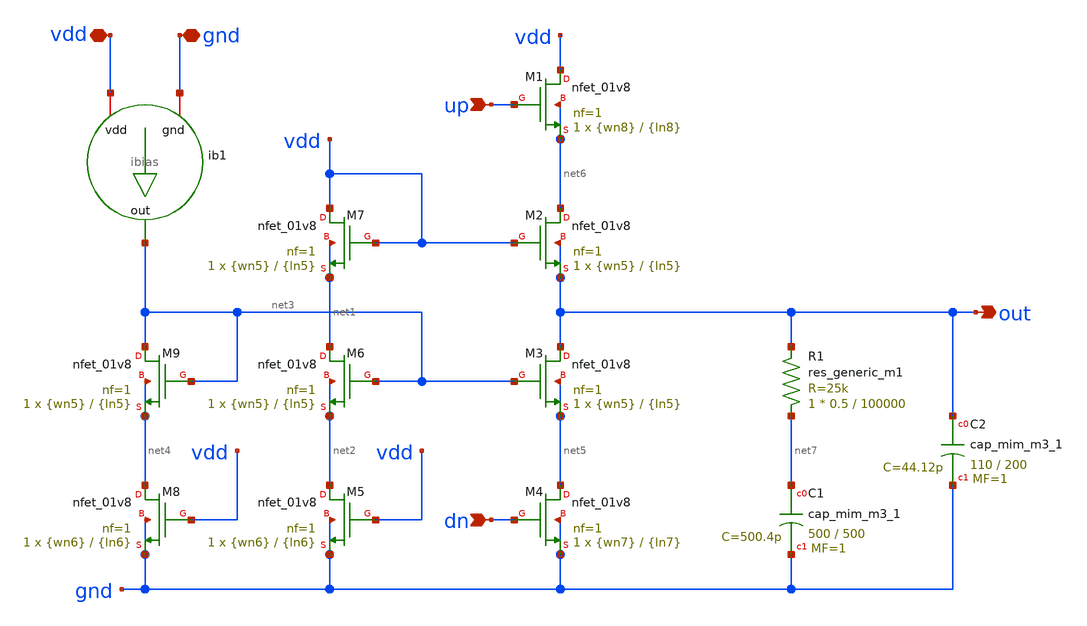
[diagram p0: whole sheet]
** sch_path: charge-pump-2/charge-pump.sch
**.subckt charge-pump vdd gnd dn up out
*.iopin vdd
*.iopin gnd
*.ipin dn
*.ipin up
*.opin out
XM1 vdd up net6 net6 sky130_fd_pr__nfet_01v8 L={ln8} W={wn8} nf=1 ad='int((nf+1)/2) * W/nf * 0.29' as='int((nf+2)/2) * W/nf * 0.29'
+ pd='2*int((nf+1)/2) * (W/nf + 0.29)' ps='2*int((nf+2)/2) * (W/nf + 0.29)' nrd='0.29 / W' nrs='0.29 / W'
+ sa=0 sb=0 sd=0 mult=1 m=1
XM2 net6 vdd out out sky130_fd_pr__nfet_01v8 L={ln5} W={wn5} nf=1 ad='int((nf+1)/2) * W/nf * 0.29' as='int((nf+2)/2) * W/nf * 0.29'
+ pd='2*int((nf+1)/2) * (W/nf + 0.29)' ps='2*int((nf+2)/2) * (W/nf + 0.29)' nrd='0.29 / W' nrs='0.29 / W'
+ sa=0 sb=0 sd=0 mult=1 m=1
XM3 out net3 net5 net5 sky130_fd_pr__nfet_01v8 L={ln5} W={wn5} nf=1 ad='int((nf+1)/2) * W/nf * 0.29'
+ as='int((nf+2)/2) * W/nf * 0.29' pd='2*int((nf+1)/2) * (W/nf + 0.29)' ps='2*int((nf+2)/2) * (W/nf + 0.29)'
+ nrd='0.29 / W' nrs='0.29 / W' sa=0 sb=0 sd=0 mult=1 m=1
XM4 net5 dn gnd gnd sky130_fd_pr__nfet_01v8 L={ln7} W={wn7} nf=1 ad='int((nf+1)/2) * W/nf * 0.29' as='int((nf+2)/2) * W/nf * 0.29'
+ pd='2*int((nf+1)/2) * (W/nf + 0.29)' ps='2*int((nf+2)/2) * (W/nf + 0.29)' nrd='0.29 / W' nrs='0.29 / W'
+ sa=0 sb=0 sd=0 mult=1 m=1
XM5 net2 vdd gnd gnd sky130_fd_pr__nfet_01v8 L={ln6} W={wn6} nf=1 ad='int((nf+1)/2) * W/nf * 0.29' as='int((nf+2)/2) * W/nf * 0.29'
+ pd='2*int((nf+1)/2) * (W/nf + 0.29)' ps='2*int((nf+2)/2) * (W/nf + 0.29)' nrd='0.29 / W' nrs='0.29 / W'
+ sa=0 sb=0 sd=0 mult=1 m=1
XM6 net1 net3 net2 net2 sky130_fd_pr__nfet_01v8 L={ln5} W={wn5} nf=1 ad='int((nf+1)/2) * W/nf * 0.29'
+ as='int((nf+2)/2) * W/nf * 0.29' pd='2*int((nf+1)/2) * (W/nf + 0.29)' ps='2*int((nf+2)/2) * (W/nf + 0.29)'
+ nrd='0.29 / W' nrs='0.29 / W' sa=0 sb=0 sd=0 mult=1 m=1
XM7 vdd vdd net1 net1 sky130_fd_pr__nfet_01v8 L={ln5} W={wn5} nf=1 ad='int((nf+1)/2) * W/nf * 0.29' as='int((nf+2)/2) * W/nf * 0.29'
+ pd='2*int((nf+1)/2) * (W/nf + 0.29)' ps='2*int((nf+2)/2) * (W/nf + 0.29)' nrd='0.29 / W' nrs='0.29 / W'
+ sa=0 sb=0 sd=0 mult=1 m=1
XM8 net4 vdd gnd gnd sky130_fd_pr__nfet_01v8 L={ln6} W={wn6} nf=1 ad='int((nf+1)/2) * W/nf * 0.29' as='int((nf+2)/2) * W/nf * 0.29'
+ pd='2*int((nf+1)/2) * (W/nf + 0.29)' ps='2*int((nf+2)/2) * (W/nf + 0.29)' nrd='0.29 / W' nrs='0.29 / W'
+ sa=0 sb=0 sd=0 mult=1 m=1
XM9 net3 net3 net4 net4 sky130_fd_pr__nfet_01v8 L={ln5} W={wn5} nf=1 ad='int((nf+1)/2) * W/nf * 0.29'
+ as='int((nf+2)/2) * W/nf * 0.29' pd='2*int((nf+1)/2) * (W/nf + 0.29)' ps='2*int((nf+2)/2) * (W/nf + 0.29)'
+ nrd='0.29 / W' nrs='0.29 / W' sa=0 sb=0 sd=0 mult=1 m=1
ib1 vdd net3 gnd ibias
R1 net7 out sky130_fd_pr__res_generic_m1 W=0.5 L=100000 m=1
XC1 net7 gnd sky130_fd_pr__cap_mim_m3_1 W=500 L=500 MF=1 m=1
XC2 out gnd sky130_fd_pr__cap_mim_m3_1 W=110 L=200 MF=1 m=1
**.ends
.end
